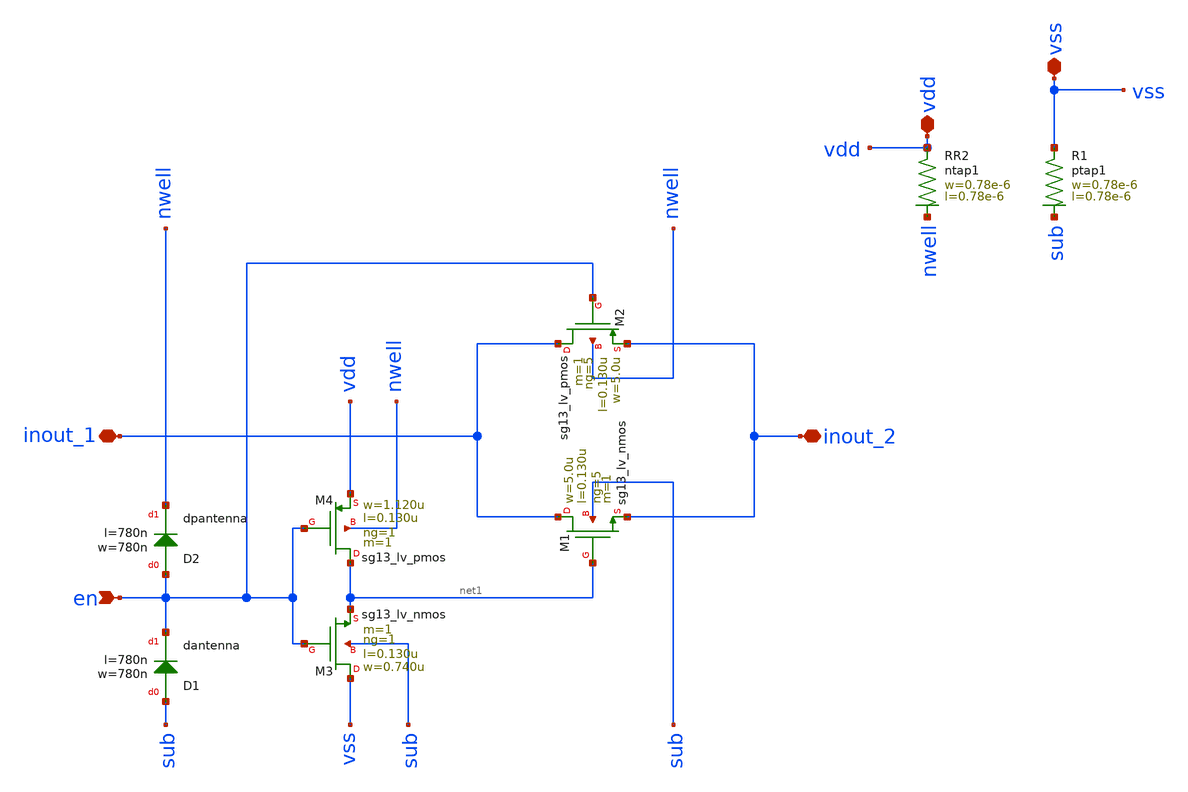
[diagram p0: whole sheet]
** sch_path: ts_pr_May2024/design_data/xschem/tgate.sch
**.subckt tgate inout_1 inout_2 en vdd vss
*.iopin inout_1
*.iopin inout_2
*.ipin en
*.iopin vdd
*.iopin vss
XM1 inout_1 net1 inout_2 sub sg13_lv_nmos w=5.0u l=0.130u ng=5 m=1 mm_ok=1
XM2 inout_1 en inout_2 nwell sg13_lv_pmos w=5.0u l=0.130u ng=5 m=1 mm_ok=1
XR1 vss sub ptap1 R=262.8 w=0.78e-6 l=0.78e-6
XR2 vdd nwell ntap1 R=262.8 w=0.78e-6 l=0.78e-6
XM3 vss en net1 sub sg13_lv_nmos w=0.740u l=0.130u ng=1 m=1 mm_ok=1
XM4 net1 en vdd nwell sg13_lv_pmos w=1.120u l=0.130u ng=1 m=1 mm_ok=1
XD1 sub en dantenna l=780n w=780n
XD2 en nwell dpantenna l=780n w=780n
**.ends
.end
